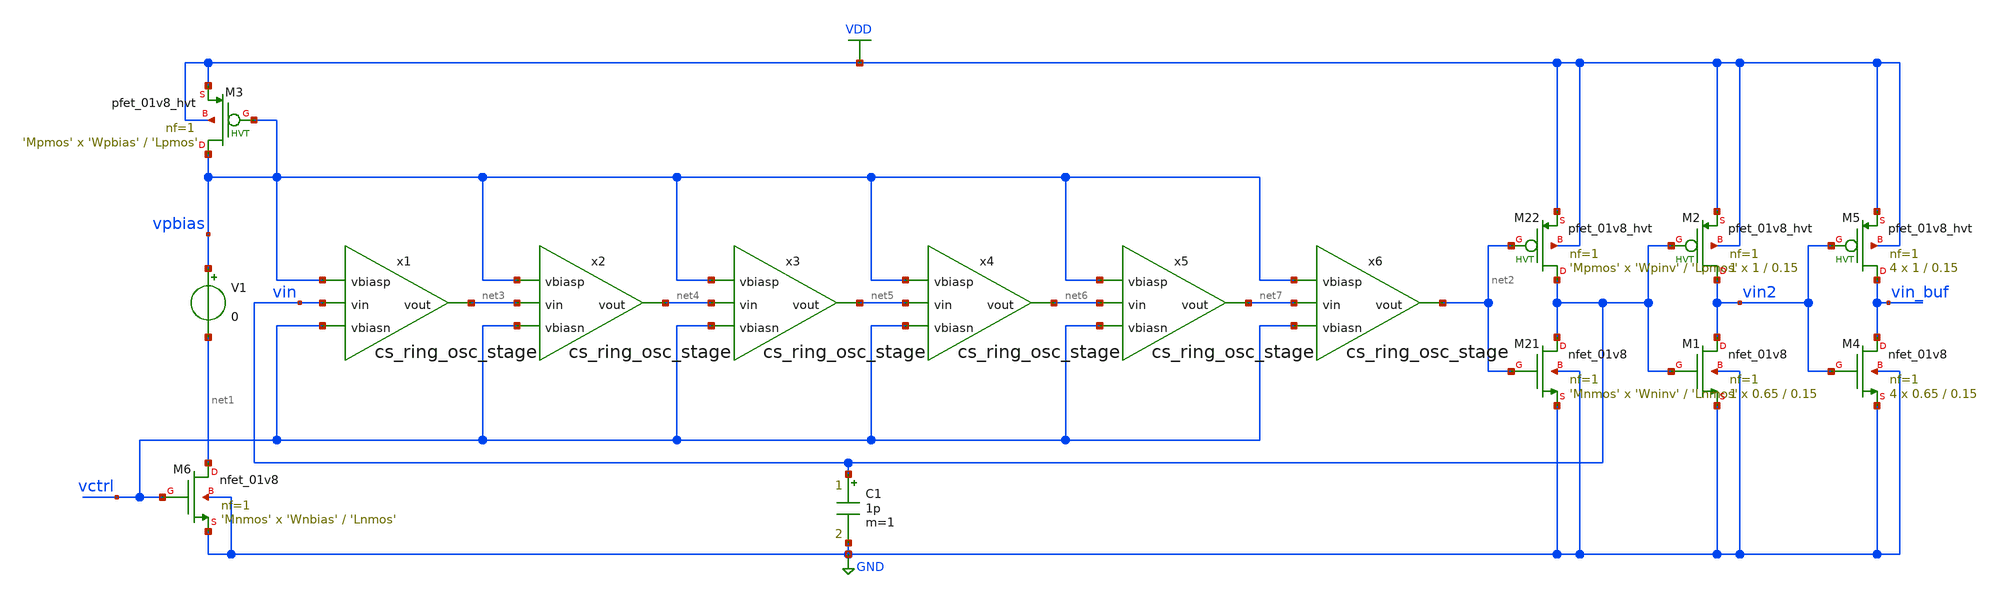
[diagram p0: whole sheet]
** sch_path: designs/dff_test.sch
* Copyright 2020 Stefan Frederik Schippers
* Licensed under the Apache License, Version 2.0 (the "License");
* you may not use this file except in compliance with the License.
* You may obtain a copy of the License at
* https://www.apache.org/licenses/LICENSE-2.0
* Unless required by applicable law or agreed to in writing, software
* distributed under the License is distributed on an "AS IS" BASIS,
* WITHOUT WARRANTIES OR CONDITIONS OF ANY KIND, either express or implied.
* See the License for the specific language governing permissions and
* limitations under the License.
**.subckt dff_test
V1 vpbias net1 0
XM6 net1 vctrl GND GND sky130_fd_pr__nfet_01v8 L='Lnmos' W='Wnbias' nf=1 ad='int((nf+1)/2) * W/nf * 0.29'
+ as='int((nf+2)/2) * W/nf * 0.29' pd='2*int((nf+1)/2) * (W/nf + 0.29)' ps='2*int((nf+2)/2) * (W/nf + 0.29)'
+ nrd='0.29 / W' nrs='0.29 / W' sa=0 sb=0 sd=0 mult='Mnmos' m='Mnmos'
XM3 vpbias vpbias VDD VDD sky130_fd_pr__pfet_01v8_hvt L='Lpmos' W='Wpbias' nf=1 ad='int((nf+1)/2) * W/nf * 0.29'
+ as='int((nf+2)/2) * W/nf * 0.29' pd='2*int((nf+1)/2) * (W/nf + 0.29)' ps='2*int((nf+2)/2) * (W/nf + 0.29)'
+ nrd='0.29 / W' nrs='0.29 / W' sa=0 sb=0 sd=0 mult='Mpmos' m='Mpmos'
x1 vpbias net3 vin vctrl cs_ring_osc_stage
x2 vpbias net4 net3 vctrl cs_ring_osc_stage
x3 vpbias net5 net4 vctrl cs_ring_osc_stage
x4 vpbias net6 net5 vctrl cs_ring_osc_stage
x5 vpbias net7 net6 vctrl cs_ring_osc_stage
x6 vpbias net2 net7 vctrl cs_ring_osc_stage
XM21 vin net2 GND GND sky130_fd_pr__nfet_01v8 L='Lnmos' W='Wninv' nf=1 ad='int((nf+1)/2) * W/nf * 0.29'
+ as='int((nf+2)/2) * W/nf * 0.29' pd='2*int((nf+1)/2) * (W/nf + 0.29)' ps='2*int((nf+2)/2) * (W/nf + 0.29)'
+ nrd='0.29 / W' nrs='0.29 / W' sa=0 sb=0 sd=0 mult='Mnmos' m='Mnmos'
XM22 vin net2 VDD VDD sky130_fd_pr__pfet_01v8_hvt L='Lpmos' W='Wpinv' nf=1 ad='int((nf+1)/2) * W/nf * 0.29'
+ as='int((nf+2)/2) * W/nf * 0.29' pd='2*int((nf+1)/2) * (W/nf + 0.29)' ps='2*int((nf+2)/2) * (W/nf + 0.29)'
+ nrd='0.29 / W' nrs='0.29 / W' sa=0 sb=0 sd=0 mult='Mpmos' m='Mpmos'
C1 vin GND 1p m=1
XM1 vin2 vin GND GND sky130_fd_pr__nfet_01v8 L=0.15 W=0.65 nf=1 ad='int((nf+1)/2) * W/nf * 0.29' as='int((nf+2)/2) * W/nf * 0.29'
+ pd='2*int((nf+1)/2) * (W/nf + 0.29)' ps='2*int((nf+2)/2) * (W/nf + 0.29)' nrd='0.29 / W' nrs='0.29 / W'
+ sa=0 sb=0 sd=0 mult=1 m=1
XM2 vin2 vin VDD VDD sky130_fd_pr__pfet_01v8_hvt L=0.15 W=1 nf=1 ad='int((nf+1)/2) * W/nf * 0.29' as='int((nf+2)/2) * W/nf * 0.29'
+ pd='2*int((nf+1)/2) * (W/nf + 0.29)' ps='2*int((nf+2)/2) * (W/nf + 0.29)' nrd='0.29 / W' nrs='0.29 / W'
+ sa=0 sb=0 sd=0 mult=1 m=1
XM4 vin_buf vin2 GND GND sky130_fd_pr__nfet_01v8 L=0.15 W=0.65 nf=1 ad='int((nf+1)/2) * W/nf * 0.29'
+ as='int((nf+2)/2) * W/nf * 0.29' pd='2*int((nf+1)/2) * (W/nf + 0.29)' ps='2*int((nf+2)/2) * (W/nf + 0.29)'
+ nrd='0.29 / W' nrs='0.29 / W' sa=0 sb=0 sd=0 mult=4 m=4
XM5 vin_buf vin2 VDD VDD sky130_fd_pr__pfet_01v8_hvt L=0.15 W=1 nf=1 ad='int((nf+1)/2) * W/nf * 0.29'
+ as='int((nf+2)/2) * W/nf * 0.29' pd='2*int((nf+1)/2) * (W/nf + 0.29)' ps='2*int((nf+2)/2) * (W/nf + 0.29)'
+ nrd='0.29 / W' nrs='0.29 / W' sa=0 sb=0 sd=0 mult=4 m=4
**** begin user architecture code

.include $::SKYWATER_MODELS/cells/nfet_01v8/sky130_fd_pr__nfet_01v8__tt.corner.spice
.include $::SKYWATER_MODELS/cells/nfet_01v8_lvt/sky130_fd_pr__nfet_01v8_lvt__tt.corner.spice
.include $::SKYWATER_MODELS/cells/pfet_01v8/sky130_fd_pr__pfet_01v8__tt.corner.spice
.include $::SKYWATER_MODELS/cells/nfet_03v3_nvt/sky130_fd_pr__nfet_03v3_nvt__tt.corner.spice
.include $::SKYWATER_MODELS/cells/nfet_05v0_nvt/sky130_fd_pr__nfet_05v0_nvt__tt.corner.spice
.include $::SKYWATER_MODELS/cells/esd_nfet_01v8/sky130_fd_pr__esd_nfet_01v8__tt.corner.spice
.include $::SKYWATER_MODELS/cells/pfet_01v8_lvt/sky130_fd_pr__pfet_01v8_lvt__tt.corner.spice
.include $::SKYWATER_MODELS/cells/pfet_01v8_hvt/sky130_fd_pr__pfet_01v8_hvt__tt.corner.spice
.include $::SKYWATER_MODELS/cells/esd_pfet_g5v0d10v5/sky130_fd_pr__esd_pfet_g5v0d10v5__tt.corner.spice
.include $::SKYWATER_MODELS/cells/pfet_g5v0d10v5/sky130_fd_pr__pfet_g5v0d10v5__tt.corner.spice
.include $::SKYWATER_MODELS/cells/pfet_g5v0d16v0/sky130_fd_pr__pfet_g5v0d16v0__tt.corner.spice
.include $::SKYWATER_MODELS/cells/nfet_g5v0d10v5/sky130_fd_pr__nfet_g5v0d10v5__tt.corner.spice
.include $::SKYWATER_MODELS/cells/nfet_g5v0d16v0/sky130_fd_pr__nfet_g5v0d16v0__tt_discrete.corner.spice
.include $::SKYWATER_MODELS/cells/esd_nfet_g5v0d10v5/sky130_fd_pr__esd_nfet_g5v0d10v5__tt.corner.spice
.include $::SKYWATER_MODELS/models/corners/tt/nonfet.spice
* Standard cells
.include $::SKYWATER_STDCELLS/cells/dfxbp/sky130_fd_sc_hd__dfxbp_1.spice
.include $::SKYWATER_STDCELLS/cells/dfxbp/sky130_fd_sc_hd__dfxbp_2.spice
* Mismatch parameters
.include $::SKYWATER_MODELS/cells/nfet_01v8/sky130_fd_pr__nfet_01v8__mismatch.corner.spice
.include $::SKYWATER_MODELS/cells/pfet_01v8/sky130_fd_pr__pfet_01v8__mismatch.corner.spice
.include $::SKYWATER_MODELS/cells/nfet_01v8_lvt/sky130_fd_pr__nfet_01v8_lvt__mismatch.corner.spice
.include $::SKYWATER_MODELS/cells/pfet_01v8_lvt/sky130_fd_pr__pfet_01v8_lvt__mismatch.corner.spice
.include $::SKYWATER_MODELS/cells/pfet_01v8_hvt/sky130_fd_pr__pfet_01v8_hvt__mismatch.corner.spice
.include $::SKYWATER_MODELS/cells/nfet_g5v0d10v5/sky130_fd_pr__nfet_g5v0d10v5__mismatch.corner.spice
.include $::SKYWATER_MODELS/cells/pfet_g5v0d10v5/sky130_fd_pr__pfet_g5v0d10v5__mismatch.corner.spice
.include $::SKYWATER_MODELS/cells/nfet_05v0_nvt/sky130_fd_pr__nfet_05v0_nvt__mismatch.corner.spice
.include $::SKYWATER_MODELS/cells/nfet_03v3_nvt/sky130_fd_pr__nfet_03v3_nvt__mismatch.corner.spice
* Resistor$::SKYWATER_MODELS/Capacitor
.include $::SKYWATER_MODELS/models/r+c/res_typical__cap_typical.spice
.include $::SKYWATER_MODELS/models/r+c/res_typical__cap_typical__lin.spice
* Special cells
.include $::SKYWATER_MODELS/models/corners/tt/specialized_cells.spice
* All models
.include $::SKYWATER_MODELS/models/all.spice
* Corner
.include $::SKYWATER_MODELS/models/corners/tt/rf.spice

**** end user architecture code
**.ends
.GLOBAL VDD
.GLOBAL GND
**** begin user architecture code

.include dff_test_commands.spice

**** end user architecture code
.end
